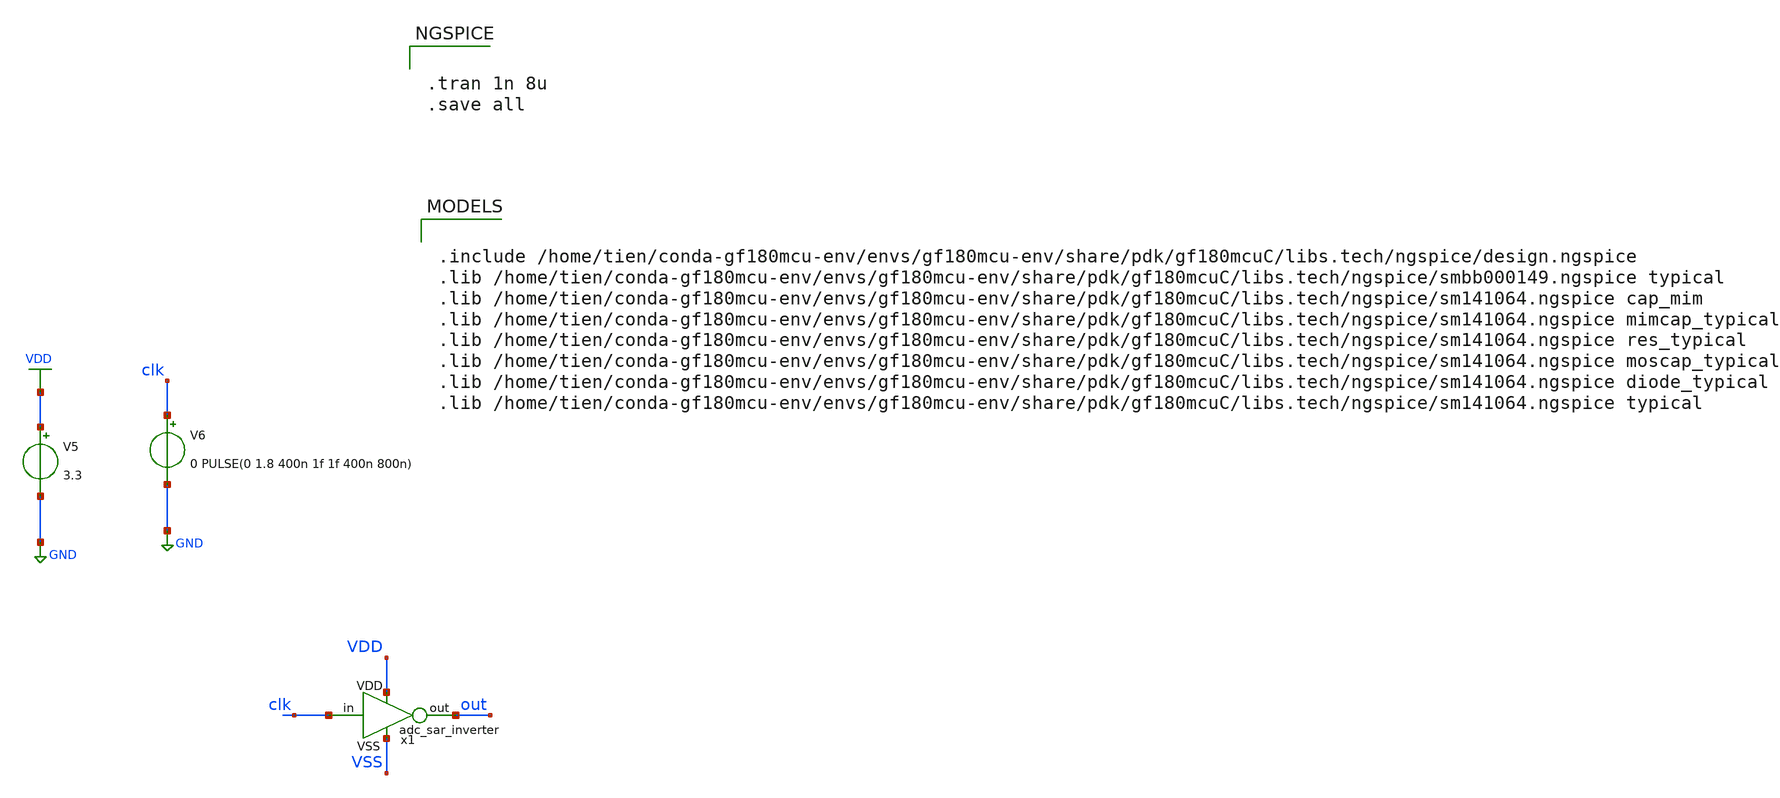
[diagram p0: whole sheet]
** sch_path: test.sch
**.subckt test
x1 VDD VSS clk out adc_sar_inverter
V5 VDD GND 3.3
V6 clk GND 0 PULSE(0 1.8 400n 1f 1f 400n 800n)
**** begin user architecture code


.tran 1n 8u
.save all



.include /home/tien/conda-gf180mcu-env/envs/gf180mcu-env/share/pdk/gf180mcuC/libs.tech/ngspice/design.ngspice
.lib /home/tien/conda-gf180mcu-env/envs/gf180mcu-env/share/pdk/gf180mcuC/libs.tech/ngspice/smbb000149.ngspice typical
.lib /home/tien/conda-gf180mcu-env/envs/gf180mcu-env/share/pdk/gf180mcuC/libs.tech/ngspice/sm141064.ngspice cap_mim
.lib /home/tien/conda-gf180mcu-env/envs/gf180mcu-env/share/pdk/gf180mcuC/libs.tech/ngspice/sm141064.ngspice mimcap_typical
.lib /home/tien/conda-gf180mcu-env/envs/gf180mcu-env/share/pdk/gf180mcuC/libs.tech/ngspice/sm141064.ngspice res_typical
.lib /home/tien/conda-gf180mcu-env/envs/gf180mcu-env/share/pdk/gf180mcuC/libs.tech/ngspice/sm141064.ngspice moscap_typical
.lib /home/tien/conda-gf180mcu-env/envs/gf180mcu-env/share/pdk/gf180mcuC/libs.tech/ngspice/sm141064.ngspice diode_typical
.lib /home/tien/conda-gf180mcu-env/envs/gf180mcu-env/share/pdk/gf180mcuC/libs.tech/ngspice/sm141064.ngspice typical

**** end user architecture code
**.ends

* expanding   symbol:  adc_sar_inverter.sym # of pins=4
** sym_path: adc_sar_inverter.sym
** sch_path: adc_sar_inverter.sch
.subckt adc_sar_inverter VDD VSS in out
*.iopin VDD
*.iopin VSS
*.ipin in
*.opin out
XM1 out in VSS VSS nfet_03v3 L=0.28u W=0.42u nf=1 ad='int((nf+1)/2) * W/nf * 0.18u' as='int((nf+2)/2) * W/nf * 0.18u'
+ pd='2*int((nf+1)/2) * (W/nf + 0.18u)' ps='2*int((nf+2)/2) * (W/nf + 0.18u)' nrd='0.18u / W' nrs='0.18u / W'
+ sa=0 sb=0 sd=0 m=1
XM2 out in VDD VDD pfet_03v3 L=0.28u W=0.84u nf=1 ad='int((nf+1)/2) * W/nf * 0.18u' as='int((nf+2)/2) * W/nf * 0.18u'
+ pd='2*int((nf+1)/2) * (W/nf + 0.18u)' ps='2*int((nf+2)/2) * (W/nf + 0.18u)' nrd='0.18u / W' nrs='0.18u / W'
+ sa=0 sb=0 sd=0 m=1
.ends

.GLOBAL GND
.GLOBAL VDD
.end
